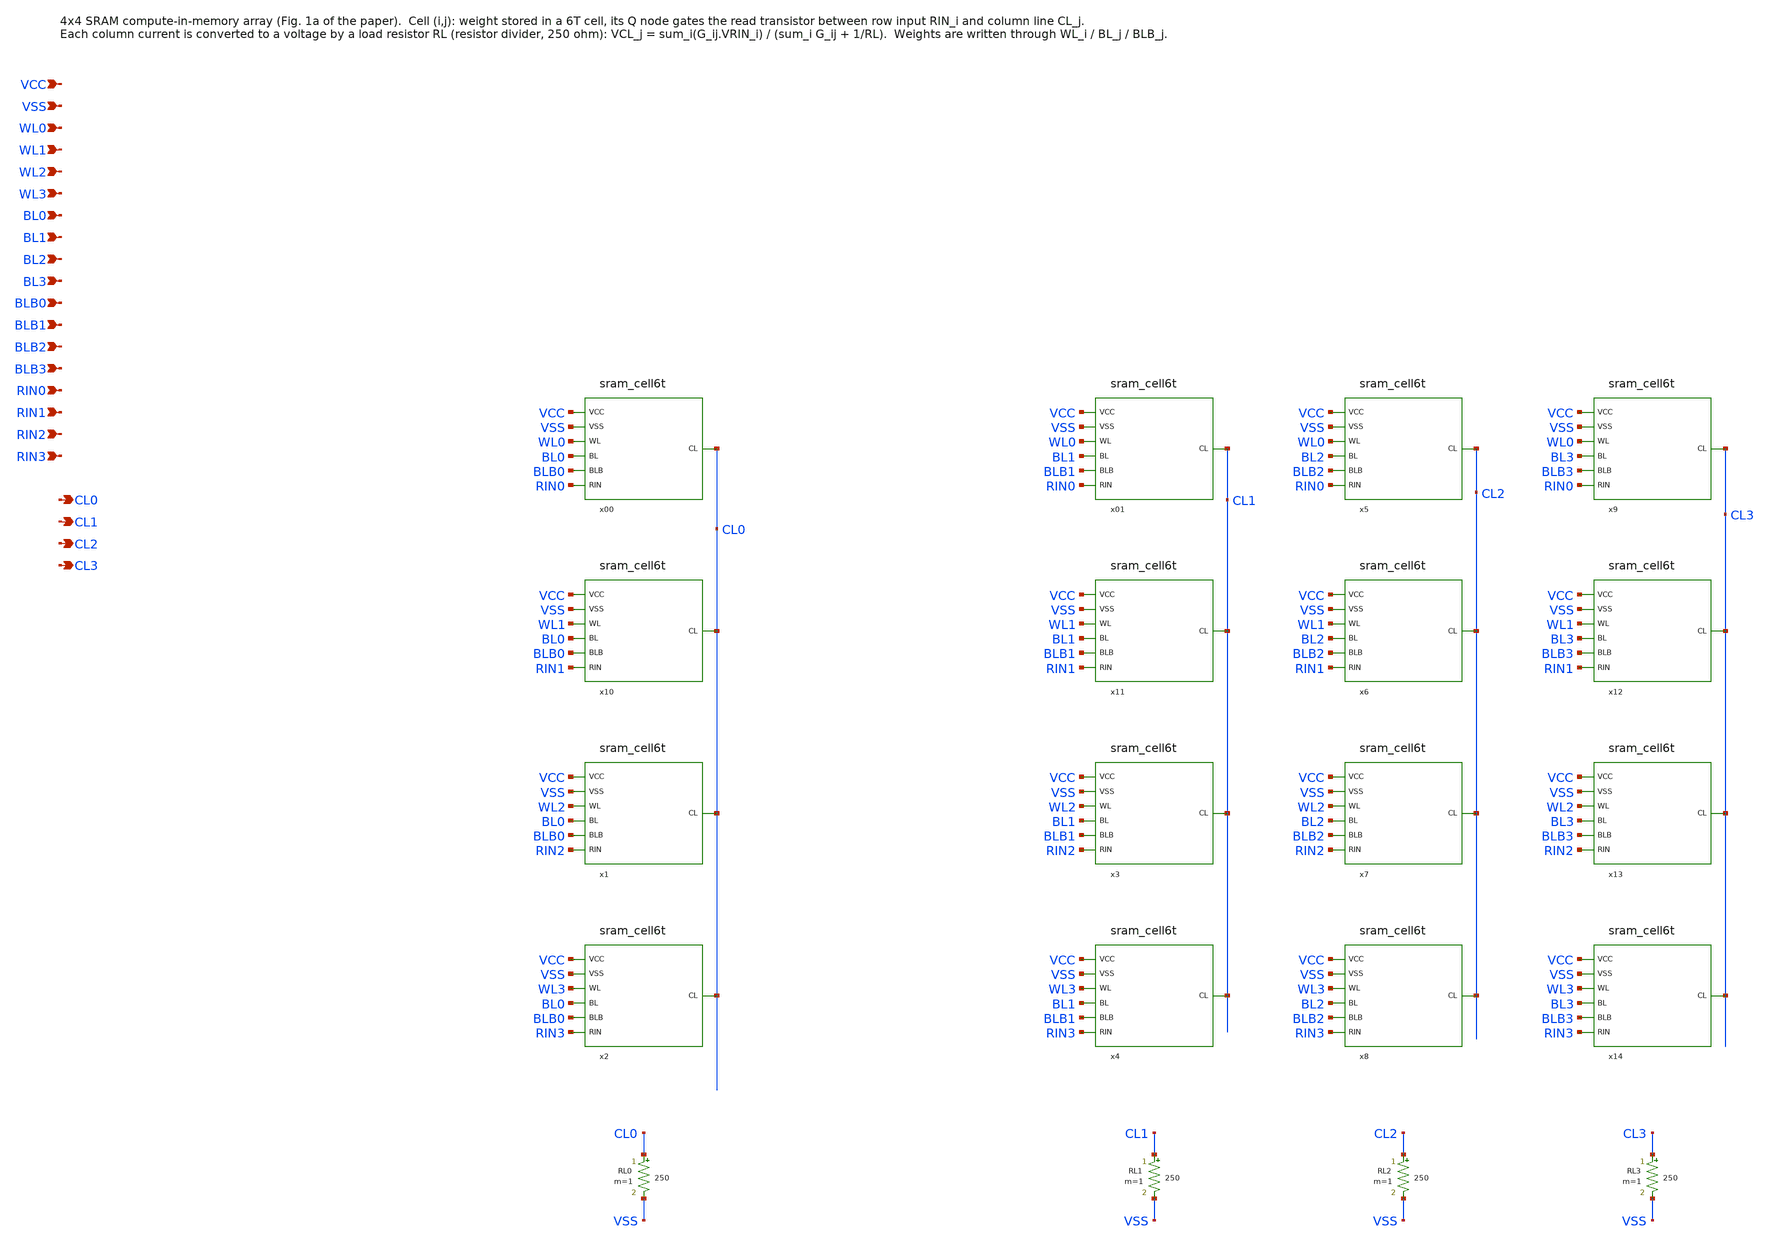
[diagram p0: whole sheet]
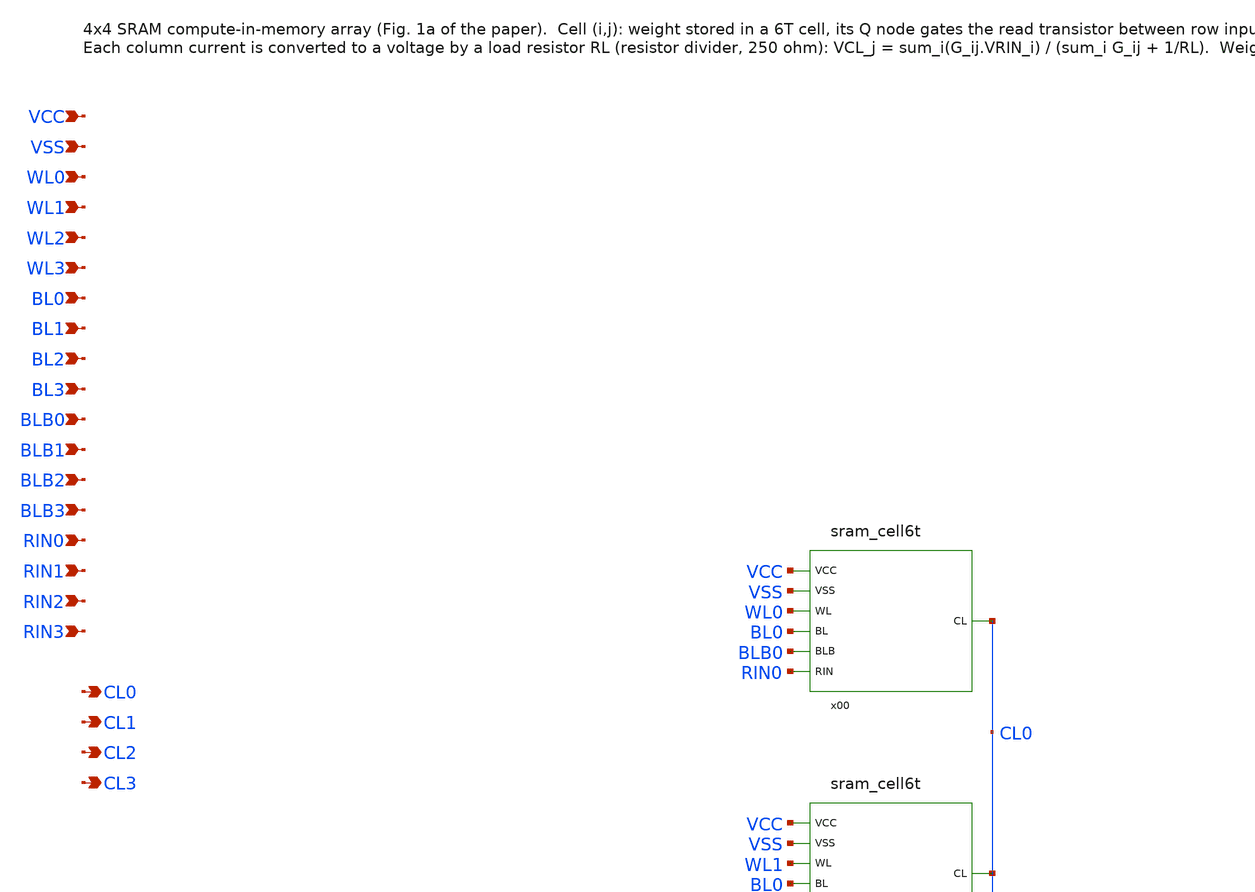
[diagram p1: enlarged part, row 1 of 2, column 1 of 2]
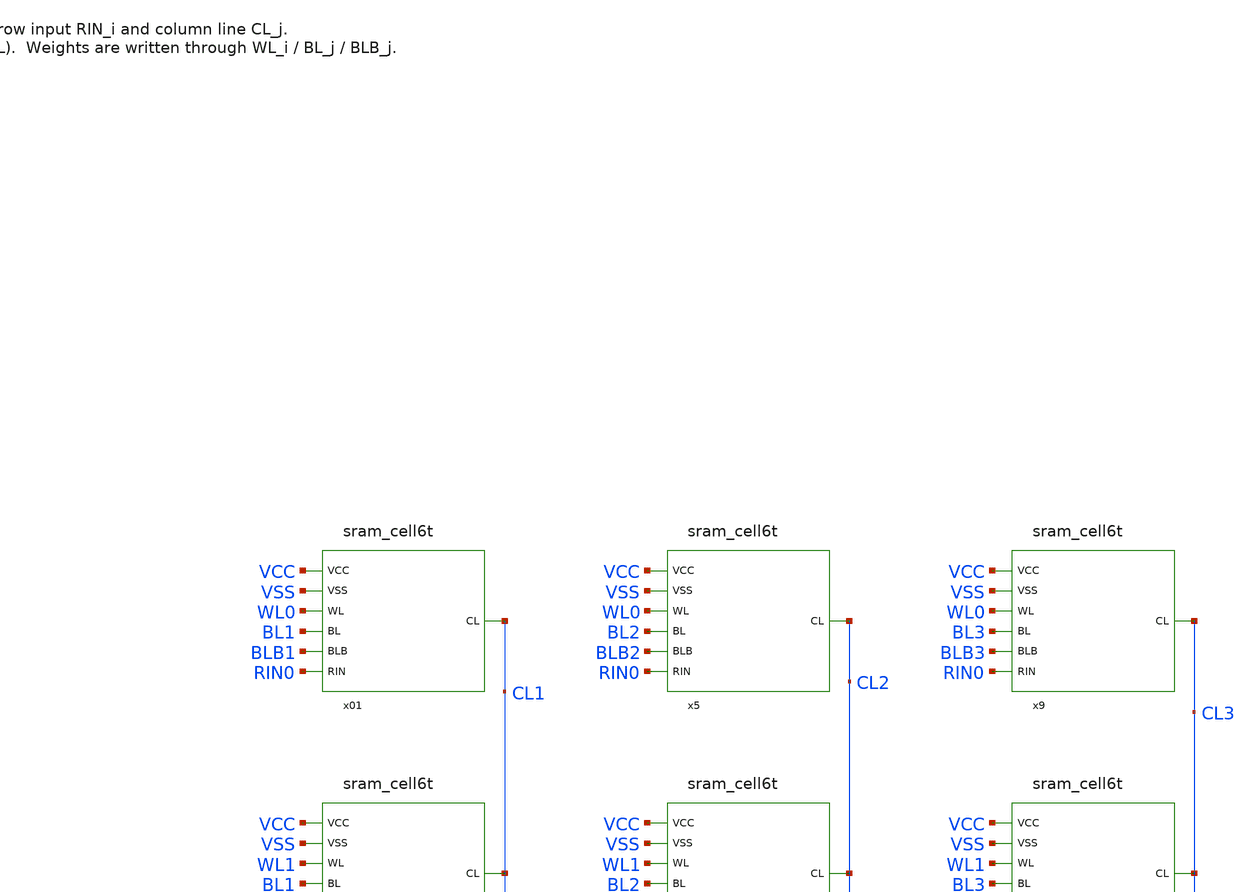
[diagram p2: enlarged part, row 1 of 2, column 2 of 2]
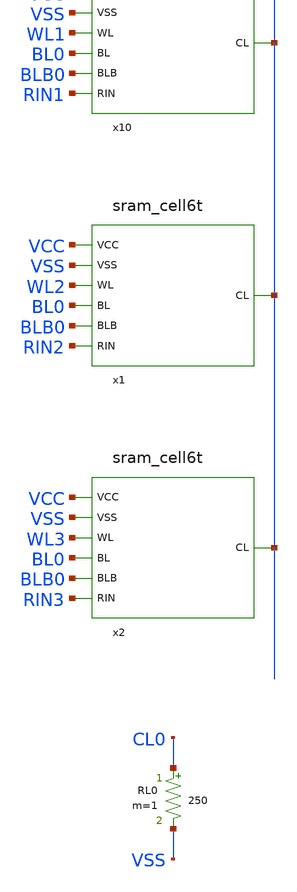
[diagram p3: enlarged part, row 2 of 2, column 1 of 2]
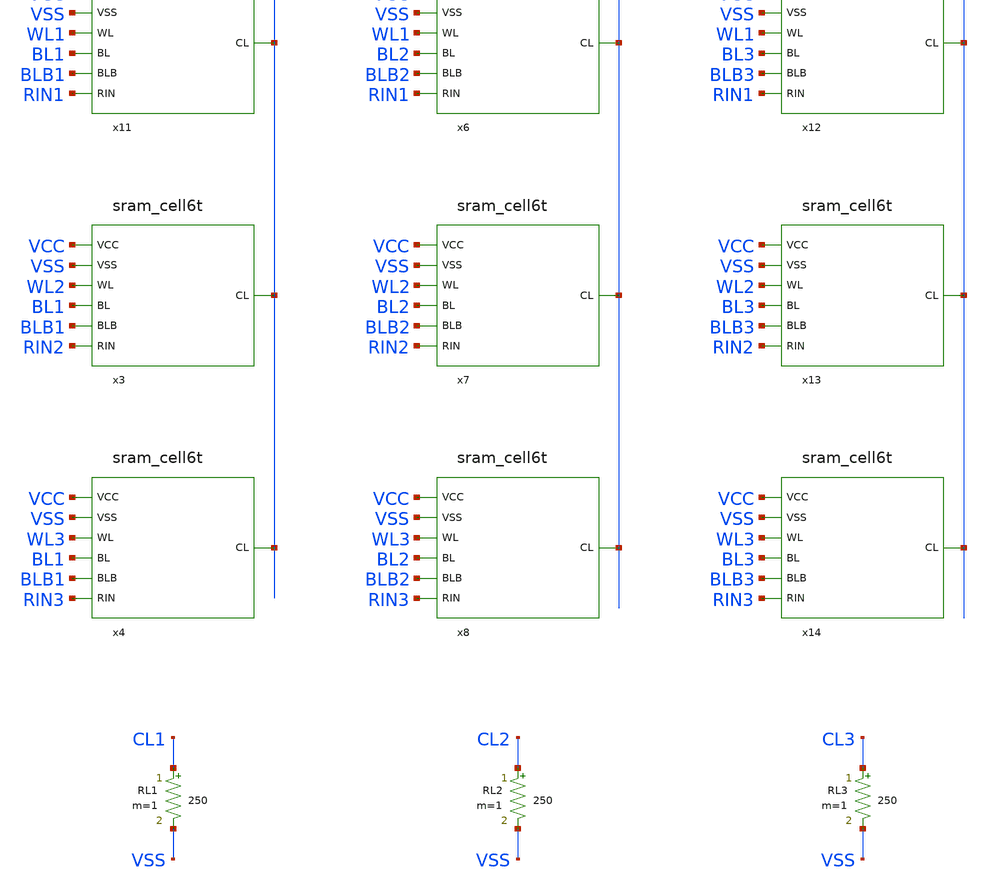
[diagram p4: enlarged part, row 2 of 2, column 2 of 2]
** sch_path: CiM components/cim_sram_4x4.sch
**.subckt cim_sram_4x4 VCC VSS WL0 WL1 WL2 WL3 BL0 BL1 BL2 BL3 BLB0 BLB1 BLB2 BLB3 RIN0 RIN1 RIN2
*+ RIN3 CL0 CL1 CL2 CL3
*.ipin VCC
*.ipin VSS
*.ipin WL0
*.ipin WL1
*.ipin WL2
*.ipin WL3
*.ipin BL0
*.ipin BL1
*.ipin BL2
*.ipin BL3
*.ipin BLB0
*.ipin BLB1
*.ipin BLB2
*.ipin BLB3
*.ipin RIN0
*.ipin RIN1
*.ipin RIN2
*.ipin RIN3
*.opin CL0
*.opin CL1
*.opin CL2
*.opin CL3
x00 VCC VSS WL0 BL0 BLB0 RIN0 CL0 sram_cell6t
x01 VCC VSS WL0 BL1 BLB1 RIN0 CL1 sram_cell6t
x10 VCC VSS WL1 BL0 BLB0 RIN1 CL0 sram_cell6t
x11 VCC VSS WL1 BL1 BLB1 RIN1 CL1 sram_cell6t
RL0 CL0 VSS 250 m=1
RL1 CL1 VSS 250 m=1
RL2 CL2 VSS 250 m=1
RL3 CL3 VSS 250 m=1
x1 VCC VSS WL2 BL0 BLB0 RIN2 CL0 sram_cell6t
x2 VCC VSS WL3 BL0 BLB0 RIN3 CL0 sram_cell6t
x3 VCC VSS WL2 BL1 BLB1 RIN2 CL1 sram_cell6t
x4 VCC VSS WL3 BL1 BLB1 RIN3 CL1 sram_cell6t
x5 VCC VSS WL0 BL2 BLB2 RIN0 CL2 sram_cell6t
x6 VCC VSS WL1 BL2 BLB2 RIN1 CL2 sram_cell6t
x7 VCC VSS WL2 BL2 BLB2 RIN2 CL2 sram_cell6t
x8 VCC VSS WL3 BL2 BLB2 RIN3 CL2 sram_cell6t
x9 VCC VSS WL0 BL3 BLB3 RIN0 CL3 sram_cell6t
x12 VCC VSS WL1 BL3 BLB3 RIN1 CL3 sram_cell6t
x13 VCC VSS WL2 BL3 BLB3 RIN2 CL3 sram_cell6t
x14 VCC VSS WL3 BL3 BLB3 RIN3 CL3 sram_cell6t
**.ends

* expanding   symbol:  /home/ttuser/Documents/ADCAnalogDesign/CiM components/sram_cell6t.sym # of
*+ pins=7
** sym_path: CiM components/sram_cell6t.sym
** sch_path: CiM components/sram_cell6t.sch
.subckt sram_cell6t VCC VSS WL BL BLB RIN CL
*.ipin VCC
*.ipin VSS
*.ipin WL
*.ipin BL
*.ipin BLB
*.ipin RIN
*.opin CL
XMPU1 Q QB VCC VCC sky130_fd_pr__pfet_01v8 L=0.15 W=0.42 nf=1 ad='int((nf+1)/2) * W/nf * 0.29' as='int((nf+2)/2) * W/nf * 0.29'
+ pd='2*int((nf+1)/2) * (W/nf + 0.29)' ps='2*int((nf+2)/2) * (W/nf + 0.29)' nrd='0.29 / W' nrs='0.29 / W'
+ sa=0 sb=0 sd=0 mult=1 m=1
XMPU2 QB Q VCC VCC sky130_fd_pr__pfet_01v8 L=0.15 W=0.42 nf=1 ad='int((nf+1)/2) * W/nf * 0.29' as='int((nf+2)/2) * W/nf * 0.29'
+ pd='2*int((nf+1)/2) * (W/nf + 0.29)' ps='2*int((nf+2)/2) * (W/nf + 0.29)' nrd='0.29 / W' nrs='0.29 / W'
+ sa=0 sb=0 sd=0 mult=1 m=1
XMPD1 Q QB VSS VSS sky130_fd_pr__nfet_01v8 L=0.15 W=1 nf=1 ad='int((nf+1)/2) * W/nf * 0.29' as='int((nf+2)/2) * W/nf * 0.29'
+ pd='2*int((nf+1)/2) * (W/nf + 0.29)' ps='2*int((nf+2)/2) * (W/nf + 0.29)' nrd='0.29 / W' nrs='0.29 / W'
+ sa=0 sb=0 sd=0 mult=1 m=1
XMPD2 QB Q VSS VSS sky130_fd_pr__nfet_01v8 L=0.15 W=1 nf=1 ad='int((nf+1)/2) * W/nf * 0.29' as='int((nf+2)/2) * W/nf * 0.29'
+ pd='2*int((nf+1)/2) * (W/nf + 0.29)' ps='2*int((nf+2)/2) * (W/nf + 0.29)' nrd='0.29 / W' nrs='0.29 / W'
+ sa=0 sb=0 sd=0 mult=1 m=1
XMAX1 BL WL Q VSS sky130_fd_pr__nfet_01v8 L=0.15 W=0.6 nf=1 ad='int((nf+1)/2) * W/nf * 0.29' as='int((nf+2)/2) * W/nf * 0.29'
+ pd='2*int((nf+1)/2) * (W/nf + 0.29)' ps='2*int((nf+2)/2) * (W/nf + 0.29)' nrd='0.29 / W' nrs='0.29 / W'
+ sa=0 sb=0 sd=0 mult=1 m=1
XMAX2 BLB WL QB VSS sky130_fd_pr__nfet_01v8 L=0.15 W=0.6 nf=1 ad='int((nf+1)/2) * W/nf * 0.29' as='int((nf+2)/2) * W/nf * 0.29'
+ pd='2*int((nf+1)/2) * (W/nf + 0.29)' ps='2*int((nf+2)/2) * (W/nf + 0.29)' nrd='0.29 / W' nrs='0.29 / W'
+ sa=0 sb=0 sd=0 mult=1 m=1
XMRD RIN Q CL VSS sky130_fd_pr__nfet_01v8 L=0.15 W=0.5 nf=1 ad='int((nf+1)/2) * W/nf * 0.29' as='int((nf+2)/2) * W/nf * 0.29'
+ pd='2*int((nf+1)/2) * (W/nf + 0.29)' ps='2*int((nf+2)/2) * (W/nf + 0.29)' nrd='0.29 / W' nrs='0.29 / W'
+ sa=0 sb=0 sd=0 mult=1 m=1
.ends

.end
